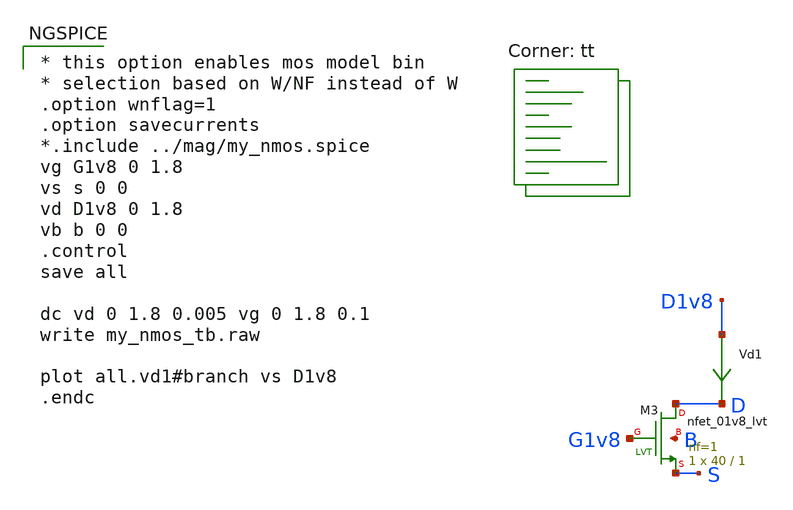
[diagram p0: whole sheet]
** sch_path: hw07/xschem/nmos_tb.sch
**.subckt nmos_tb
Vd1 D1v8 D 0
.save i(vd1)
XM3 D G1v8 S B sky130_fd_pr__nfet_01v8_lvt L=1 W=40 nf=1 ad='int((1 + 1)/2) * 40 / 1 * 0.29' as='int((1 + 2)/2) * 40 / 1 * 0.29'
+ pd='2*int((1 + 1)/2) * (40 / 1 + 0.29)' ps='2*int((1 + 2)/2) * (40 / 1 + 0.29)' nrd='0.29 / 40 ' nrs='0.29 / 40 '
+ sa=0 sb=0 sd=0 mult=1 m=1
**** begin user architecture code

* this option enables mos model bin
* selection based on W/NF instead of W
.option wnflag=1
.option savecurrents
*.include ../mag/my_nmos.spice
vg G1v8 0 1.8
vs s 0 0
vd D1v8 0 1.8
vb b 0 0
.control
save all

dc vd 0 1.8 0.005 vg 0 1.8 0.1
write my_nmos_tb.raw

plot all.vd1#branch vs D1v8
.endc


.lib $::SKYWATER_MODELS/sky130.lib.spice tt
**** end user architecture code
**.ends
.end
